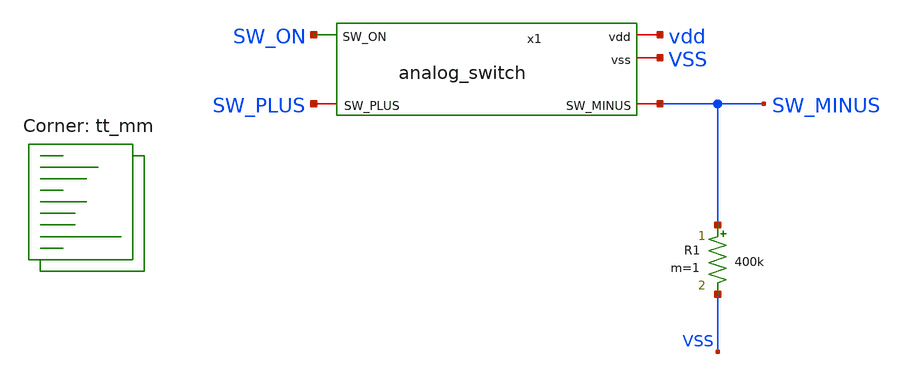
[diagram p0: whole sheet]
** sch_path: xschem/analog_switch_tb.sch
**.subckt analog_switch_tb
R1 SW_MINUS VSS 400k m=1
x1 vdd VSS SW_ON SW_PLUS SW_MINUS analog_switch
**** begin user architecture code
.lib $::SKYWATER_MODELS/sky130.lib.spice tt_mm

*.option method = gear
*.option wnflag = 1
.options gmin=1e-12 abstol=1e-12 reltol=1e-3
.options method=gear
.options maxord=2
.param VCC = 3.3
.option temp = aguass(40,30,1)
.include stimuli_tb_analog_switch.cir
.control
	option seed = 69
	let run = 0
	dowhile run <= 1
		save all
		tran 1n 8u uic
		remzerovec
		write tb_analog_switch_tran.raw
		set appendwrite
		reset
		let run = run +1
	end
.endc



**** end user architecture code
**.ends

* expanding   symbol:  analog_switch.sym # of pins=5
** sym_path: xschem/analog_switch.sym
** sch_path: xschem/analog_switch.sch
.subckt analog_switch vdd vss SW_ON SW_PLUS SW_MINUS
*.iopin vdd
*.iopin vss
*.ipin SW_ON
*.iopin SW_MINUS
*.iopin SW_PLUS
XM1 SW_PLUS SW_ON_BUF SW_MINUS SW_MINUS sky130_fd_pr__nfet_g5v0d10v5 L=15 W=16 nf=1 ad='int((1 + 1)/2) * 16 / 1 * 0.29'
+ as='int((1 + 2)/2) * 16 / 1 * 0.29' pd='2*int((1 + 1)/2) * (16 / 1 + 0.29)' ps='2*int((1 + 2)/2) * (16 / 1 + 0.29)'
+ nrd='0.29 / 16 ' nrs='0.29 / 16 ' sa=0 sb=0 sd=0 mult=1 m=1
XM3 SW_MINUS nSW_ON SW_PLUS SW_PLUS sky130_fd_pr__pfet_g5v0d10v5 L=15 W=16 nf=1 ad='int((1 + 1)/2) * 16 / 1 * 0.29'
+ as='int((1 + 2)/2) * 16 / 1 * 0.29' pd='2*int((1 + 1)/2) * (16 / 1 + 0.29)' ps='2*int((1 + 2)/2) * (16 / 1 + 0.29)'
+ nrd='0.29 / 16 ' nrs='0.29 / 16 ' sa=0 sb=0 sd=0 mult=1 m=1
XM2 SW_MINUS nSW_ON SW_MINUS SW_MINUS sky130_fd_pr__nfet_g5v0d10v5 L=15 W=16 nf=1 ad='int((1 + 1)/2) * 16 / 1 * 0.29'
+ as='int((1 + 2)/2) * 16 / 1 * 0.29' pd='2*int((1 + 1)/2) * (16 / 1 + 0.29)' ps='2*int((1 + 2)/2) * (16 / 1 + 0.29)'
+ nrd='0.29 / 16 ' nrs='0.29 / 16 ' sa=0 sb=0 sd=0 mult=1 m=1
XM4 SW_MINUS SW_ON_BUF SW_MINUS SW_MINUS sky130_fd_pr__pfet_g5v0d10v5 L=15 W=16 nf=1 ad='int((1 + 1)/2) * 16 / 1 * 0.29'
+ as='int((1 + 2)/2) * 16 / 1 * 0.29' pd='2*int((1 + 1)/2) * (16 / 1 + 0.29)' ps='2*int((1 + 2)/2) * (16 / 1 + 0.29)'
+ nrd='0.29 / 16 ' nrs='0.29 / 16 ' sa=0 sb=0 sd=0 mult=1 m=1
XM6 SW_ON_BUF net1 vss vss sky130_fd_pr__nfet_g5v0d10v5 L=0.5 W=2 nf=1 ad='int((1 + 1)/2) * 2 / 1 * 0.29'
+ as='int((1 + 2)/2) * 2 / 1 * 0.29' pd='2*int((1 + 1)/2) * (2 / 1 + 0.29)' ps='2*int((1 + 2)/2) * (2 / 1 + 0.29)'
+ nrd='0.29 / 2 ' nrs='0.29 / 2 ' sa=0 sb=0 sd=0 mult=1 m=1
XM7 SW_ON_BUF net1 vdd vdd sky130_fd_pr__pfet_g5v0d10v5 L=0.5 W=2 nf=1 ad='int((1 + 1)/2) * 2 / 1 * 0.29'
+ as='int((1 + 2)/2) * 2 / 1 * 0.29' pd='2*int((1 + 1)/2) * (2 / 1 + 0.29)' ps='2*int((1 + 2)/2) * (2 / 1 + 0.29)'
+ nrd='0.29 / 2 ' nrs='0.29 / 2 ' sa=0 sb=0 sd=0 mult=1 m=1
XM8 net1 SW_ON vss vss sky130_fd_pr__nfet_g5v0d10v5 L=0.5 W=2 nf=1 ad='int((1 + 1)/2) * 2 / 1 * 0.29'
+ as='int((1 + 2)/2) * 2 / 1 * 0.29' pd='2*int((1 + 1)/2) * (2 / 1 + 0.29)' ps='2*int((1 + 2)/2) * (2 / 1 + 0.29)'
+ nrd='0.29 / 2 ' nrs='0.29 / 2 ' sa=0 sb=0 sd=0 mult=1 m=1
XM10 net1 SW_ON vdd vdd sky130_fd_pr__pfet_g5v0d10v5 L=0.5 W=2 nf=1 ad='int((1 + 1)/2) * 2 / 1 * 0.29'
+ as='int((1 + 2)/2) * 2 / 1 * 0.29' pd='2*int((1 + 1)/2) * (2 / 1 + 0.29)' ps='2*int((1 + 2)/2) * (2 / 1 + 0.29)'
+ nrd='0.29 / 2 ' nrs='0.29 / 2 ' sa=0 sb=0 sd=0 mult=1 m=1
XM5 nSW_ON SW_ON_BUF vss vss sky130_fd_pr__nfet_g5v0d10v5 L=0.5 W=2 nf=1 ad='int((1 + 1)/2) * 2 / 1 * 0.29'
+ as='int((1 + 2)/2) * 2 / 1 * 0.29' pd='2*int((1 + 1)/2) * (2 / 1 + 0.29)' ps='2*int((1 + 2)/2) * (2 / 1 + 0.29)'
+ nrd='0.29 / 2 ' nrs='0.29 / 2 ' sa=0 sb=0 sd=0 mult=1 m=1
XM9 nSW_ON SW_ON_BUF vdd vdd sky130_fd_pr__pfet_g5v0d10v5 L=0.5 W=2 nf=1 ad='int((1 + 1)/2) * 2 / 1 * 0.29'
+ as='int((1 + 2)/2) * 2 / 1 * 0.29' pd='2*int((1 + 1)/2) * (2 / 1 + 0.29)' ps='2*int((1 + 2)/2) * (2 / 1 + 0.29)'
+ nrd='0.29 / 2 ' nrs='0.29 / 2 ' sa=0 sb=0 sd=0 mult=1 m=1
.ends

.end
